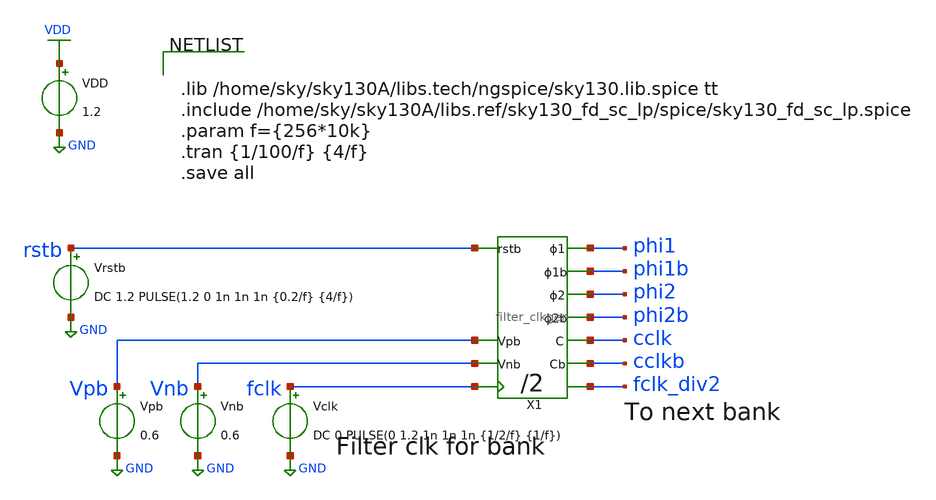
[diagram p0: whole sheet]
** sch_path: xschem/clkgen/filter_clkgen_tb.sch
**.subckt filter_clkgen_tb
Vrstb rstb GND DC 1.2 PULSE(1.2 0 1n 1n 1n {0.2/f} {4/f})
VDD VDD GND 1.2
Vpb Vpb GND 0.6
Vnb Vnb GND 0.6
Vclk fclk GND DC 0 PULSE(0 1.2 1n 1n 1n {1/2/f} {1/f})
X1 rstb fclk phi2b phi2 phi1b phi1 cclkb cclk fclk_div2 Vpb Vnb filter_clkgen
**** begin user architecture code


.lib /home/sky/sky130A/libs.tech/ngspice/sky130.lib.spice tt
.include /home/sky/sky130A/libs.ref/sky130_fd_sc_lp/spice/sky130_fd_sc_lp.spice
.param f={256*10k}
.tran {1/100/f} {4/f}
.save all


**** end user architecture code
**.ends
.GLOBAL VDD
.GLOBAL GND
.end
